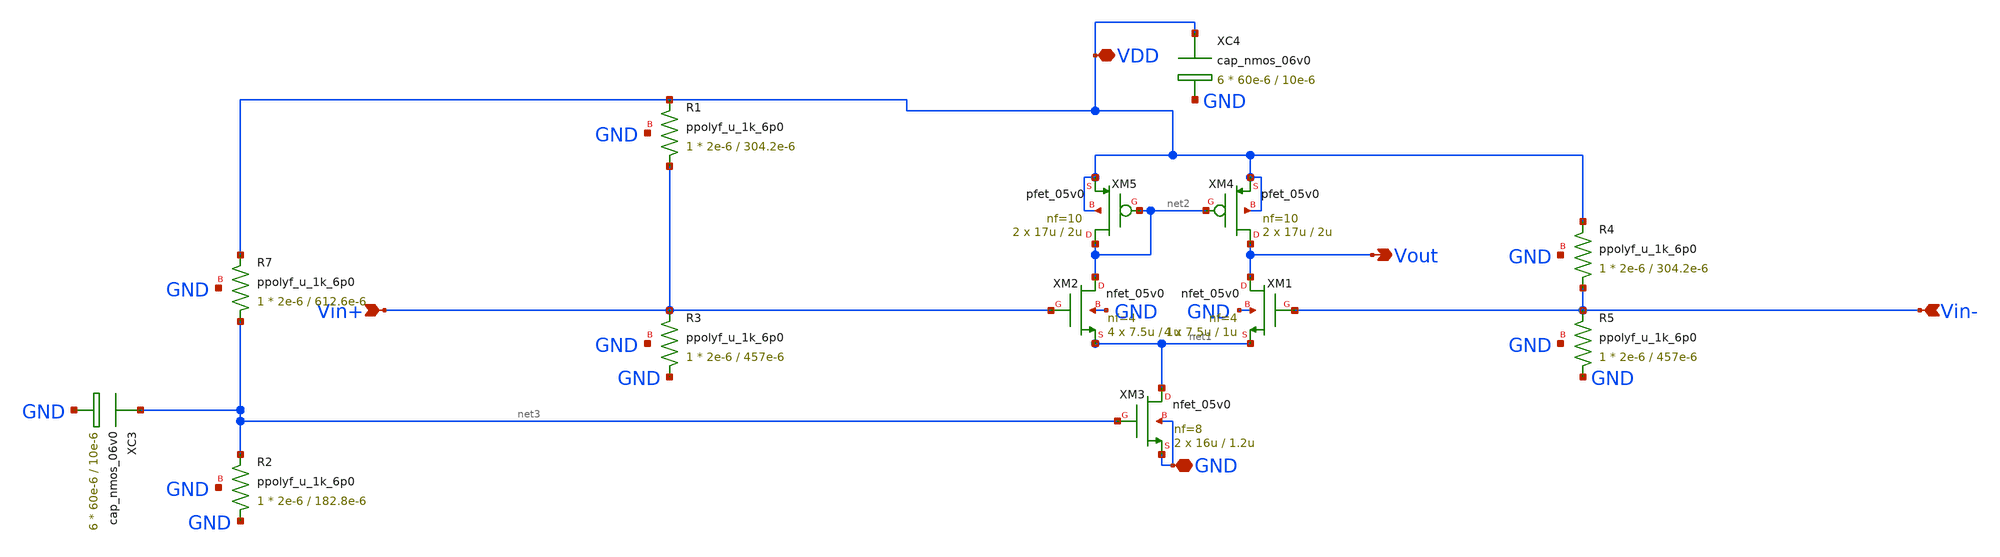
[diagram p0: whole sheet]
** sch_path: RN_Gm3/RN_gm3_ota.sch
**.subckt RN_gm3_ota Vout Vin+ Vin- VDD GND
*.opin Vout
*.ipin Vin+
*.ipin Vin-
*.iopin VDD
*.iopin GND
XM3 net1 net3 GND GND nfet_05v0 L=1.2u W=16u nf=8 ad='int((nf+1)/2) * W/nf * 0.18u' as='int((nf+2)/2) * W/nf * 0.18u'
+ pd='2*int((nf+1)/2) * (W/nf + 0.18u)' ps='2*int((nf+2)/2) * (W/nf + 0.18u)' nrd='0.18u / W' nrs='0.18u / W'
+ sa=0 sb=0 sd=0 m=2
XM2 net2 Vin+ net1 GND nfet_05v0 L=1u W=7.5u nf=4 ad='int((nf+1)/2) * W/nf * 0.18u' as='int((nf+2)/2) * W/nf * 0.18u'
+ pd='2*int((nf+1)/2) * (W/nf + 0.18u)' ps='2*int((nf+2)/2) * (W/nf + 0.18u)' nrd='0.18u / W' nrs='0.18u / W'
+ sa=0 sb=0 sd=0 m=4
XM5 net2 net2 VDD VDD pfet_05v0 L=2u W=17u nf=10 ad='int((nf+1)/2) * W/nf * 0.18u' as='int((nf+2)/2) * W/nf * 0.18u'
+ pd='2*int((nf+1)/2) * (W/nf + 0.18u)' ps='2*int((nf+2)/2) * (W/nf + 0.18u)' nrd='0.18u / W' nrs='0.18u / W'
+ sa=0 sb=0 sd=0 m=2
XC3 net3 GND cap_nmos_06v0 c_width=60e-6 c_length=10e-6 m=6
XC4 VDD GND cap_nmos_06v0 c_width=60e-6 c_length=10e-6 m=6
XM1 Vout Vin- net1 GND nfet_05v0 L=1u W=7.5u nf=4 ad='int((nf+1)/2) * W/nf * 0.18u' as='int((nf+2)/2) * W/nf * 0.18u'
+ pd='2*int((nf+1)/2) * (W/nf + 0.18u)' ps='2*int((nf+2)/2) * (W/nf + 0.18u)' nrd='0.18u / W' nrs='0.18u / W'
+ sa=0 sb=0 sd=0 m=4
XM4 Vout net2 VDD VDD pfet_05v0 L=2u W=17u nf=10 ad='int((nf+1)/2) * W/nf * 0.18u' as='int((nf+2)/2) * W/nf * 0.18u'
+ pd='2*int((nf+1)/2) * (W/nf + 0.18u)' ps='2*int((nf+2)/2) * (W/nf + 0.18u)' nrd='0.18u / W' nrs='0.18u / W'
+ sa=0 sb=0 sd=0 m=2
XR2 GND net3 GND ppolyf_u_1k_6p0 r_width=2e-6 r_length=182.8e-6 m=1
XR7 net3 VDD GND ppolyf_u_1k_6p0 r_width=2e-6 r_length=612.6e-6 m=1
XR1 Vin+ VDD GND ppolyf_u_1k_6p0 r_width=2e-6 r_length=304.2e-6 m=1
XR3 GND Vin+ GND ppolyf_u_1k_6p0 r_width=2e-6 r_length=457e-6 m=1
XR4 Vin- VDD GND ppolyf_u_1k_6p0 r_width=2e-6 r_length=304.2e-6 m=1
XR5 GND Vin- GND ppolyf_u_1k_6p0 r_width=2e-6 r_length=457e-6 m=1
**.ends
.end
